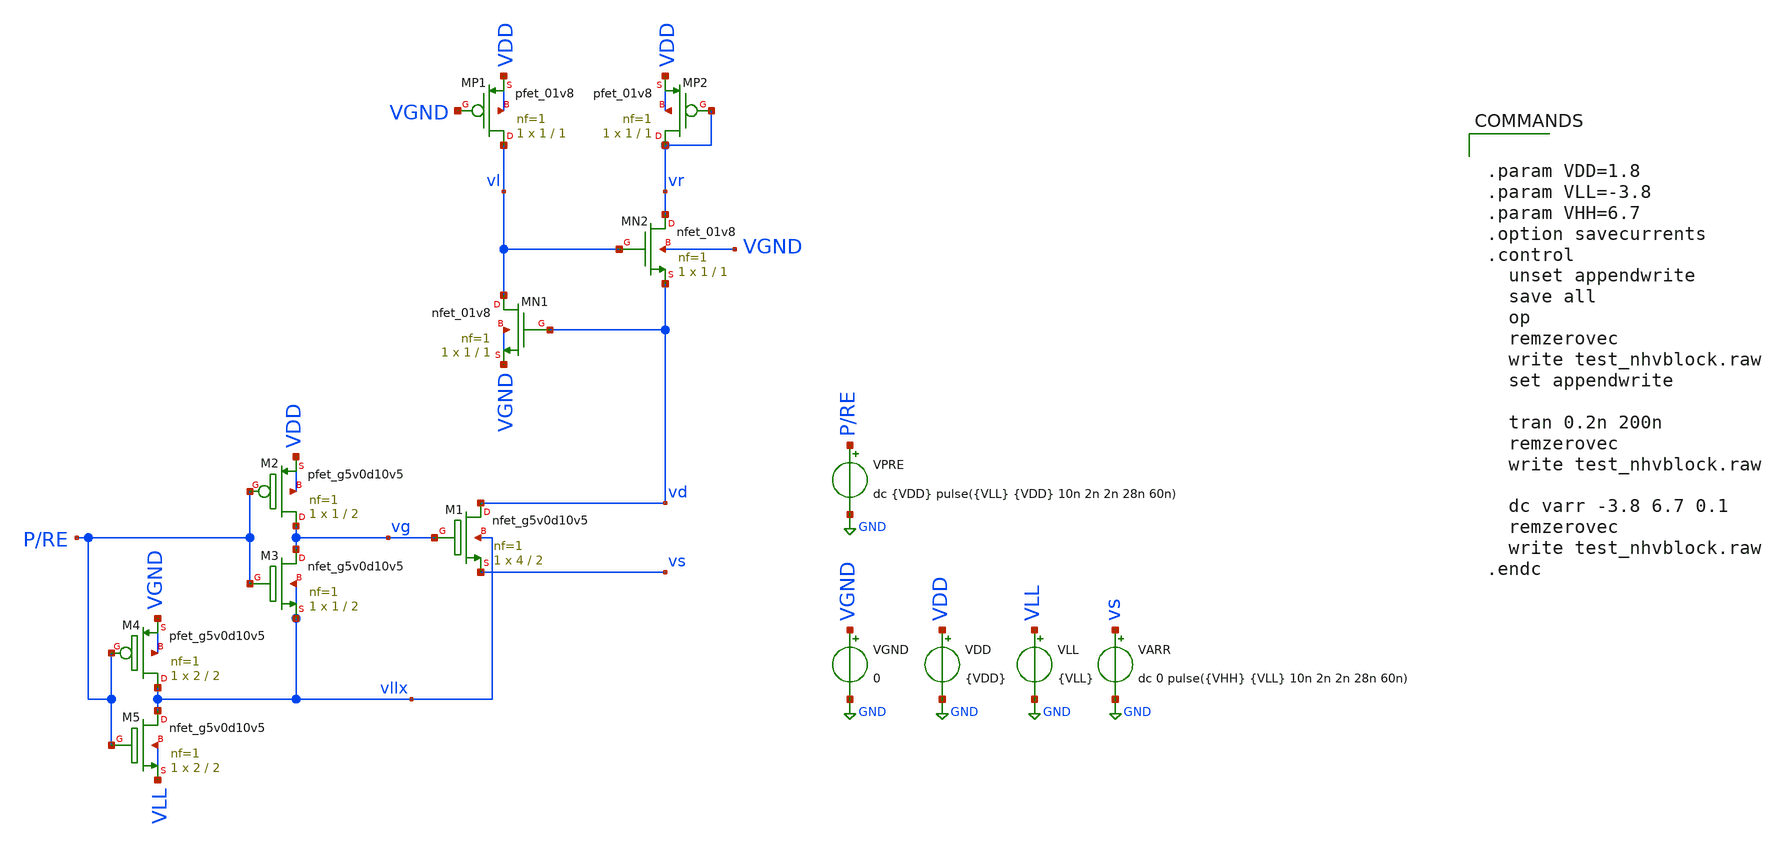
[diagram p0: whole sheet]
** sch_path: read/test_nhvblock.sch
**.subckt test_nhvblock
XM1 vd vg vs vllx sky130_fd_pr__nfet_g5v0d10v5 L=2 W=4 nf=1 ad='int((nf+1)/2) * W/nf * 0.29' as='int((nf+2)/2) * W/nf * 0.29'
+ pd='2*int((nf+1)/2) * (W/nf + 0.29)' ps='2*int((nf+2)/2) * (W/nf + 0.29)' nrd='0.29 / W' nrs='0.29 / W'
+ sa=0 sb=0 sd=0 mult=1 m=1
XM2 vg P/RE VDD VDD sky130_fd_pr__pfet_g5v0d10v5 L=2 W=1 nf=1 ad='int((nf+1)/2) * W/nf * 0.29' as='int((nf+2)/2) * W/nf * 0.29'
+ pd='2*int((nf+1)/2) * (W/nf + 0.29)' ps='2*int((nf+2)/2) * (W/nf + 0.29)' nrd='0.29 / W' nrs='0.29 / W'
+ sa=0 sb=0 sd=0 mult=1 m=1
XM3 vg P/RE vllx vllx sky130_fd_pr__nfet_g5v0d10v5 L=2 W=1 nf=1 ad='int((nf+1)/2) * W/nf * 0.29' as='int((nf+2)/2) * W/nf * 0.29'
+ pd='2*int((nf+1)/2) * (W/nf + 0.29)' ps='2*int((nf+2)/2) * (W/nf + 0.29)' nrd='0.29 / W' nrs='0.29 / W'
+ sa=0 sb=0 sd=0 mult=1 m=1
XMN1 vl vd VGND VGND sky130_fd_pr__nfet_01v8 L=1 W=1 nf=1 ad='int((nf+1)/2) * W/nf * 0.29' as='int((nf+2)/2) * W/nf * 0.29'
+ pd='2*int((nf+1)/2) * (W/nf + 0.29)' ps='2*int((nf+2)/2) * (W/nf + 0.29)' nrd='0.29 / W' nrs='0.29 / W'
+ sa=0 sb=0 sd=0 mult=1 m=1
XMP1 vl VGND VDD VDD sky130_fd_pr__pfet_01v8 L=1 W=1 nf=1 ad='int((nf+1)/2) * W/nf * 0.29' as='int((nf+2)/2) * W/nf * 0.29'
+ pd='2*int((nf+1)/2) * (W/nf + 0.29)' ps='2*int((nf+2)/2) * (W/nf + 0.29)' nrd='0.29 / W' nrs='0.29 / W'
+ sa=0 sb=0 sd=0 mult=1 m=1
XMN2 vr vl vd VGND sky130_fd_pr__nfet_01v8 L=1 W=1 nf=1 ad='int((nf+1)/2) * W/nf * 0.29' as='int((nf+2)/2) * W/nf * 0.29'
+ pd='2*int((nf+1)/2) * (W/nf + 0.29)' ps='2*int((nf+2)/2) * (W/nf + 0.29)' nrd='0.29 / W' nrs='0.29 / W'
+ sa=0 sb=0 sd=0 mult=1 m=1
XMP2 vr vr VDD VDD sky130_fd_pr__pfet_01v8 L=1 W=1 nf=1 ad='int((nf+1)/2) * W/nf * 0.29' as='int((nf+2)/2) * W/nf * 0.29'
+ pd='2*int((nf+1)/2) * (W/nf + 0.29)' ps='2*int((nf+2)/2) * (W/nf + 0.29)' nrd='0.29 / W' nrs='0.29 / W'
+ sa=0 sb=0 sd=0 mult=1 m=1
VDD VDD GND {VDD}
VGND VGND GND 0
VLL VLL GND {VLL}
VARR vs GND dc 0 pulse({VHH} {VLL} 10n 2n 2n 28n 60n)
VPRE P/RE GND dc {VDD} pulse({VLL} {VDD} 10n 2n 2n 28n 60n)
XM4 vllx P/RE VGND VGND sky130_fd_pr__pfet_g5v0d10v5 L=2 W=2 nf=1 ad='int((nf+1)/2) * W/nf * 0.29' as='int((nf+2)/2) * W/nf * 0.29'
+ pd='2*int((nf+1)/2) * (W/nf + 0.29)' ps='2*int((nf+2)/2) * (W/nf + 0.29)' nrd='0.29 / W' nrs='0.29 / W'
+ sa=0 sb=0 sd=0 mult=1 m=1
XM5 vllx P/RE VLL VLL sky130_fd_pr__nfet_g5v0d10v5 L=2 W=2 nf=1 ad='int((nf+1)/2) * W/nf * 0.29' as='int((nf+2)/2) * W/nf * 0.29'
+ pd='2*int((nf+1)/2) * (W/nf + 0.29)' ps='2*int((nf+2)/2) * (W/nf + 0.29)' nrd='0.29 / W' nrs='0.29 / W'
+ sa=0 sb=0 sd=0 mult=1 m=1
**** begin user architecture code

** opencircuitdesign pdks install
.lib $::SKYWATER_MODELS/sky130.lib.spice tt
.include $::SKYWATER_MODELS/sonos_e/begin_of_life.spice
.include $::SKYWATER_MODELS/sonos_e/begin_of_life.pm3.spice
.include $::SKYWATER_MODELS/sonos_p/begin_of_life.spice
.include $::SKYWATER_MODELS/sonos_p/begin_of_life.pm3.spice



.param VDD=1.8
.param VLL=-3.8
.param VHH=6.7
.option savecurrents
.control
  unset appendwrite
  save all
  op
  remzerovec
  write test_nhvblock.raw
  set appendwrite

  tran 0.2n 200n
  remzerovec
  write test_nhvblock.raw

  dc varr -3.8 6.7 0.1
  remzerovec
  write test_nhvblock.raw
.endc


**** end user architecture code
**.ends
.GLOBAL GND
.end
